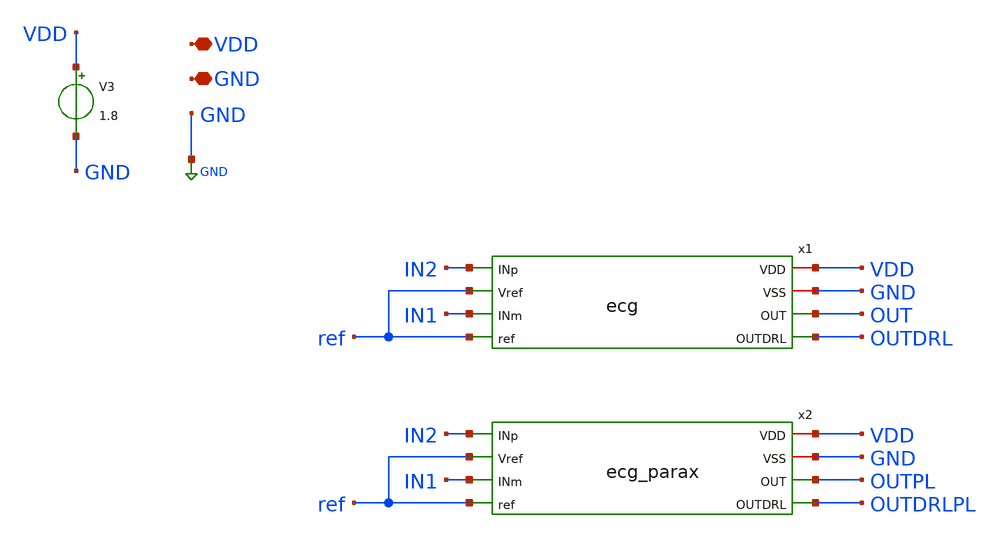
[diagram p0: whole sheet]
** sch_path: xschem/ecgPL_PWL.sch
**.subckt ecgPL_PWL VDD GND
*.iopin VDD
*.iopin GND
x1 IN2 OUT ref IN1 VDD GND ref OUTDRL ecg
x2 IN2 OUTPL ref IN1 VDD GND ref OUTDRLPL ecg_parax
V3 VDD GND 1.8
**** begin user architecture code
.lib $::SKYWATER_MODELS/sky130.lib.spice tt


 * --- DEFINIZIONE GENERATORI (Aggiornata secondo schema 2026-02-13) ---

* 1. Riferimento DC stabile a 0.9V (Nodo 'ref')
V1 ref GND 0.9

* 2. Generatore di MODO COMUNE (50Hz) connesso tra il punto comune e out_drl
* Nello schema, il morsetto negativo è su out_drl e il positivo va verso gli ingressi
VbiasR3 common_node outdrlpl dc 0 sin(0 100m 50 10u 0 0)

* 3. Braccio Positivo (ECG / 2) riferito al common_node
VbiasR1 IN1 common_node dc 0 pwl(   0.00 0.00000 0.05 0.00000 0.08 0.00000 0.10 0.00005 0.12
+ 0.000075   0.15 0.00010 0.18 0.000075 0.22 0.00000 0.28 0.00000 0.29 -0.000025   0.30 -0.00005 0.31 0.00035
+ 0.32 0.00075 0.33 0.00035 0.34 -0.00010   0.35 -0.00005 0.36 0.00000 0.40 0.00000 0.48 0.00000 0.52
+ 0.00005   0.56 0.000125 0.60 0.00015 0.64 0.000125 0.68 0.00005 0.75 0.00000   1.00 0.00000 )

* 4. Braccio Negativo (ECG / 2 Invertito) riferito al common_node
VbiasR2 IN2 common_node dc 0 pwl(   0.00 0.00000 0.05 0.00000 0.08 0.00000 0.10 -0.00005 0.12
+ -0.000075   0.15 -0.00010 0.18 -0.000075 0.22 0.00000 0.28 0.00000 0.29 0.000025   0.30 0.00005 0.31 -0.00035
+ 0.32 -0.00075 0.33 -0.00035 0.34 0.00010   0.35 0.00005 0.36 0.00000 0.40 0.00000 0.48 0.00000 0.52
+ -0.00005   0.56 -0.000125 0.60 -0.00015 0.64 -0.000125 0.68 -0.00005 0.75 0.00000   1.00 0.00000 )

* --- CONTROLLO SIMULAZIONE ---
.control
    * Nota: Assicurati che l'ingresso (+) del tuo OTA DRL sia collegato al nodo 'ref' (0.9V)
    * e l'ingresso (-) al modo comune degli elettrodi.
    set wr_vecnames
    save v(IN1) v(IN2) v(common_node) v(out_drl) v(ref) v(out) v(outpl)
    tran 10u 1.1s 0 1m

    * Visualizza come il DRL muove out_drl per annullare il 50Hz nel common_node
    plot v(common_node) v(ref) title 'Modo Comune vs Riferimento 0.9V'
    plot v(out_drl) title 'Uscita Correttiva del DRL'
    plot (v(IN1)-v(IN2)) title 'Segnale ECG Differenziale'
    plot v(out) v(outpl)


.endc



**** end user architecture code
**.ends
.GLOBAL GND
.end
